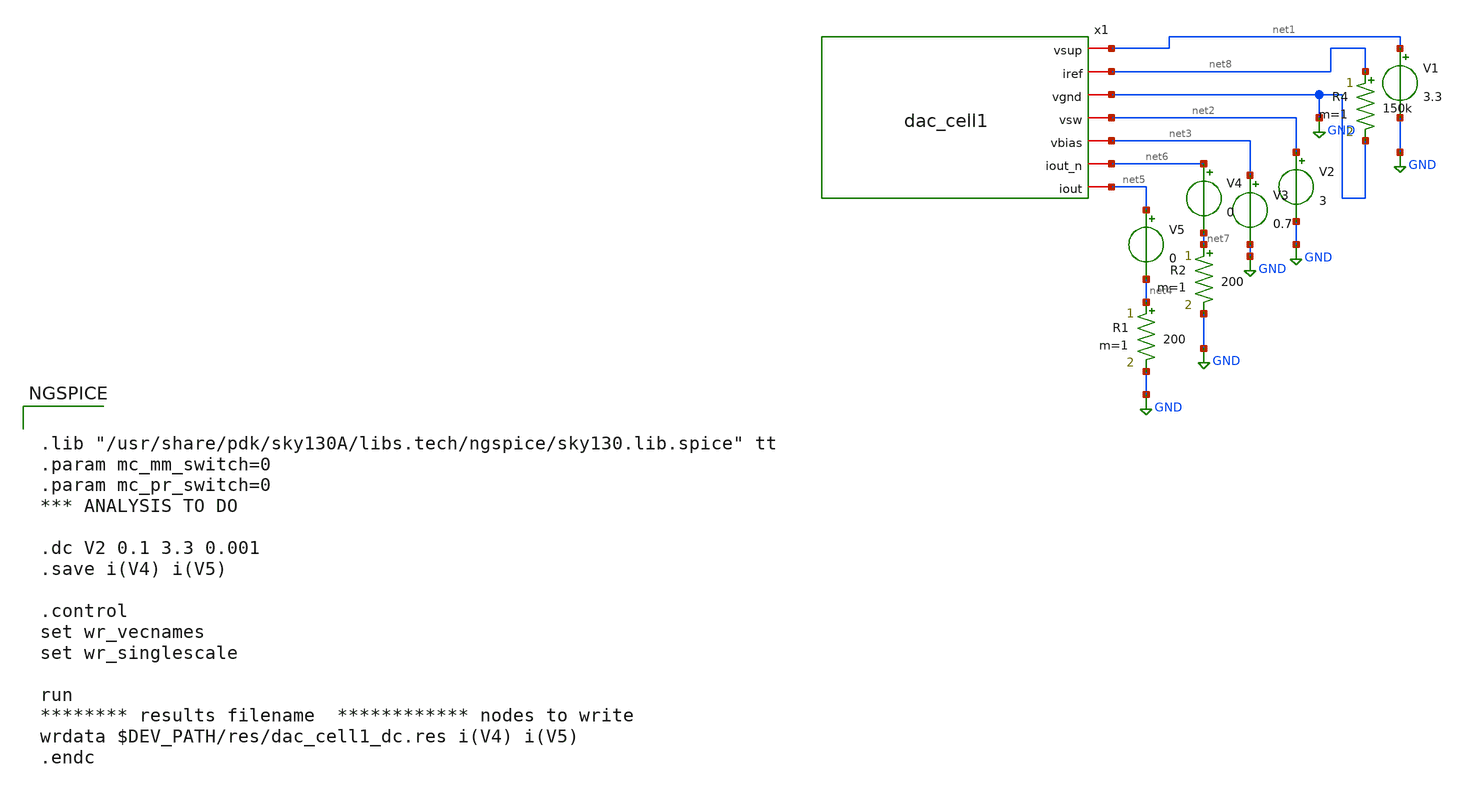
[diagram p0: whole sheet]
** sch_path: dev/dac_cell1/tb/tb_dac_cell1_dc.sch
**.subckt tb_dac_cell1_dc
V1 net1 GND 3.3
V2 net2 GND 3
V3 net3 GND 0.7
V4 net6 net7 0
V5 net5 net4 0
R1 net4 GND 200 m=1
R2 net7 GND 200 m=1
R4 net8 GND 150k m=1
x1 net1 net8 GND net2 net3 net6 net5 dac_cell1
**** begin user architecture code


.lib "/usr/share/pdk/sky130A/libs.tech/ngspice/sky130.lib.spice" tt
.param mc_mm_switch=0
.param mc_pr_switch=0
*** ANALYSIS TO DO

.dc V2 0.1 3.3 0.001
.save i(V4) i(V5)

.control
set wr_vecnames
set wr_singlescale

run
******** results filename  ************ nodes to write
wrdata $DEV_PATH/res/dac_cell1_dc.res i(V4) i(V5)
.endc


**** end user architecture code
**.ends
.GLOBAL GND
.end
